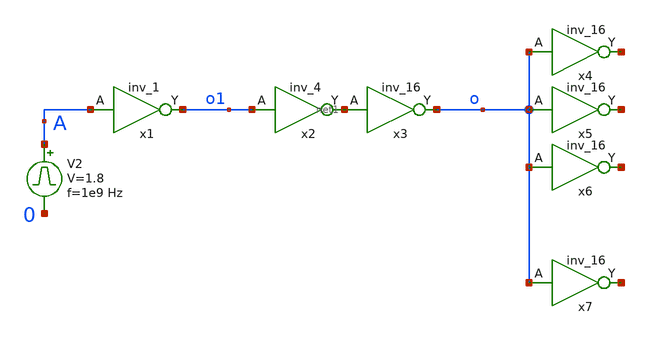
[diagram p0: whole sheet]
** sch_path: xschem/FO4_test.sch
**.subckt FO4_test
V2 A 0 pulse 0 1.8 '0.495/ 1e9 ' '0.01/1e9 ' '0.01/1e9 ' '0.49/1e9 ' '1/1e9 '
x1 A 0 0 vcc vcc o1 sky130_fd_sc_hd__inv_1
x2 o1 0 0 vcc vcc net1 sky130_fd_sc_hd__inv_4
x3 net1 0 0 vcc vcc o sky130_fd_sc_hd__inv_16
x4 o 0 0 vcc vcc net2 sky130_fd_sc_hd__inv_16
x5 o 0 0 vcc vcc net3 sky130_fd_sc_hd__inv_16
x6 o 0 0 vcc vcc net4 sky130_fd_sc_hd__inv_16
x7 o 0 0 vcc vcc net5 sky130_fd_sc_hd__inv_16
**** begin user architecture code


.options acct list
.temp 25
vvcc vcc 0 dc 1.8
vvss vss 0 0
.control
tran 1p 2n
plot a b+2 clk+4 reset_b+6 x+8 y+10 q+12 qlatch+14
write test_stdcells.raw
.endc


 .lib $::SKYWATER_MODELS/sky130.lib.spice tt
.include $::SKYWATER_STDCELLS/sky130_fd_sc_hd.spice

**** end user architecture code
**.ends
.end
